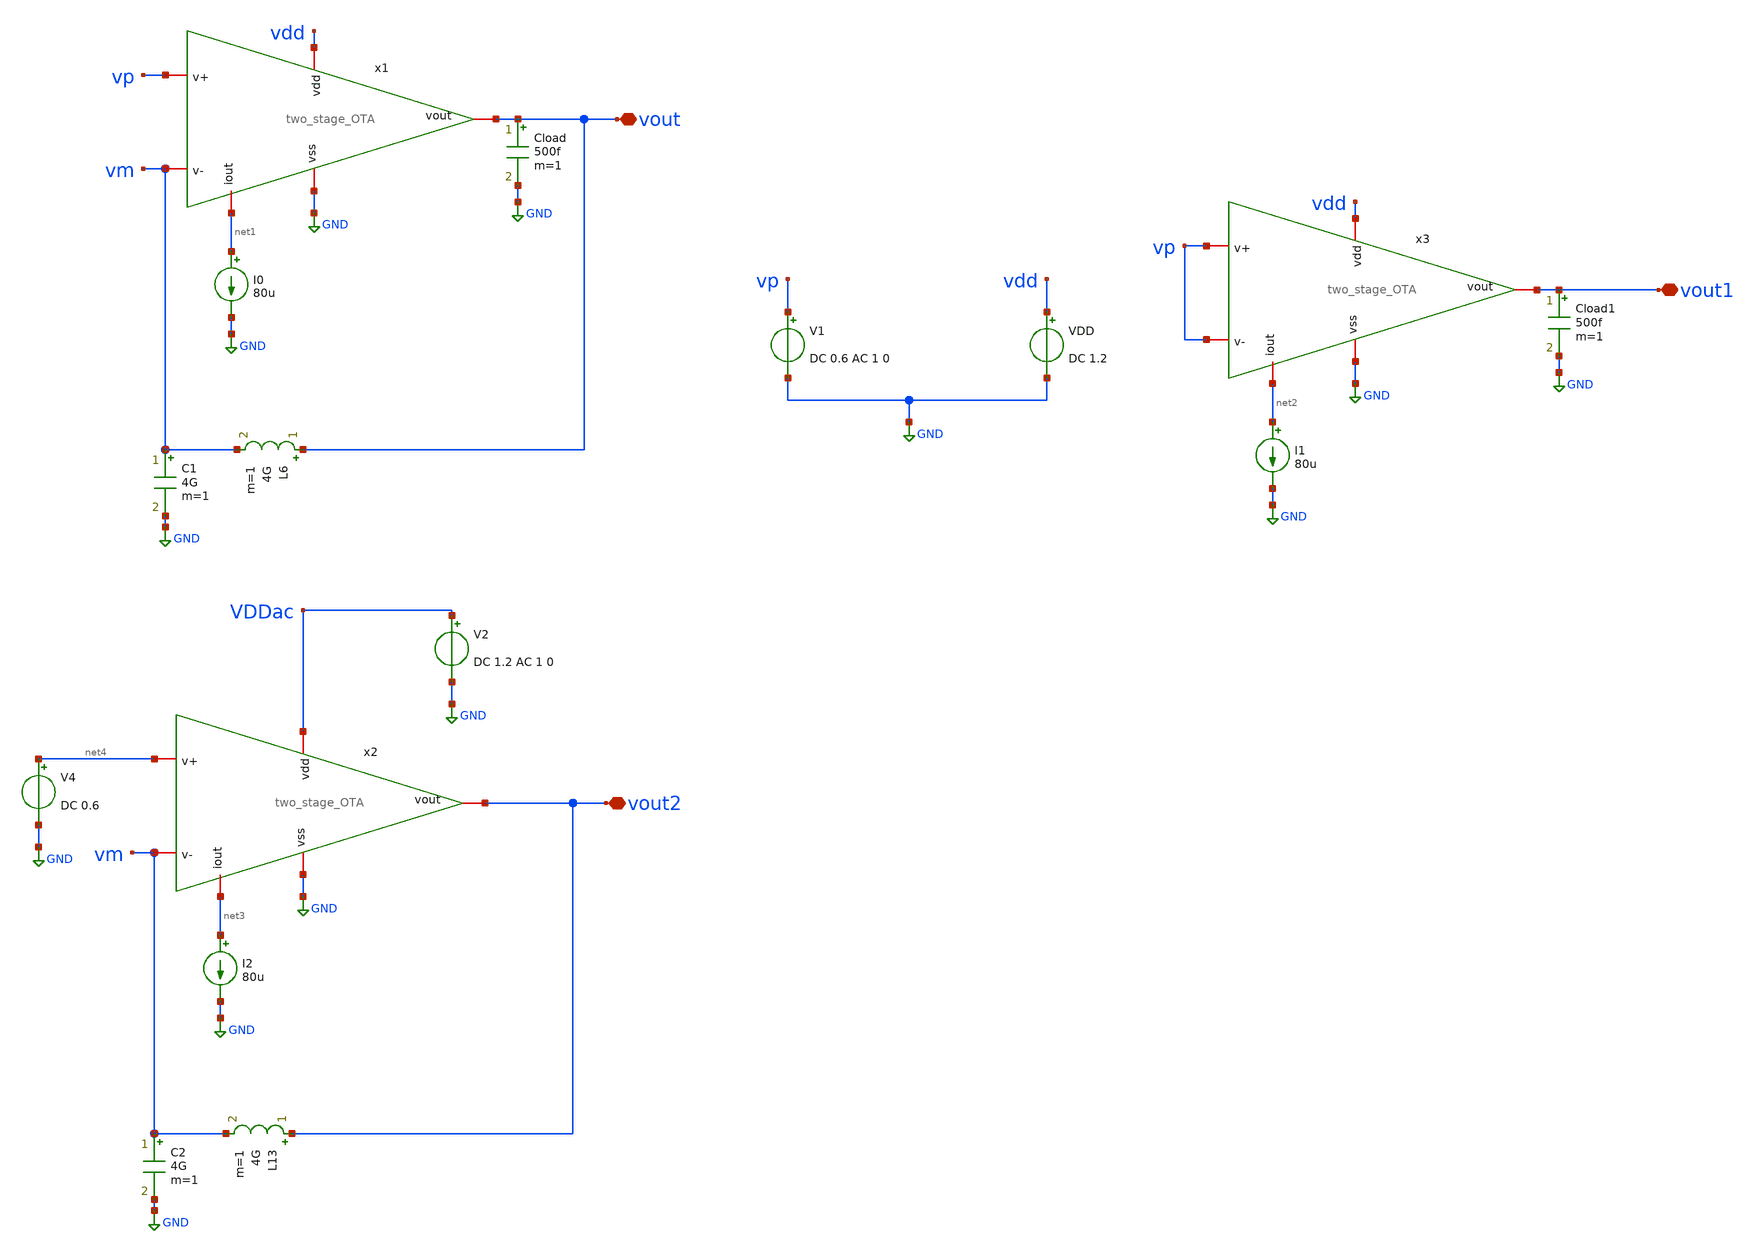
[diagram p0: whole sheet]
** sch_path: modules/module_1_bandgap_reference/part_1_OTA/testbenches/ota_testbench.sch
**.subckt ota_testbench vout vout1 vout2
*.iopin vout
*.iopin vout1
*.iopin vout2
V1 vp GND DC 0.6 AC 1 0
VDD vdd GND DC 1.2
I0 net1 GND 80u
Cload vout GND 500f m=1
L6 vout vm 4G m=1
C1 vm GND 4G m=1
I1 net2 GND 80u
Cload1 vout1 GND 500f m=1
I2 net3 GND 80u
L13 vout2 vm 4G m=1
C2 vm GND 4G m=1
V2 VDDac GND DC 1.2 AC 1 0
V4 net4 GND DC 0.6
x1 vdd net1 vp vm vout GND two_stage_OTA
x2 VDDac net3 net4 vm vout2 GND two_stage_OTA
x3 vdd net2 vp vp vout1 GND two_stage_OTA
**** begin user architecture code

.lib $::SG13G2_MODELS/cornerCAP.lib cap_typ
.lib cornerMOSlv.lib mos_tt



.control
op
save all
write tb_OTA_op.raw
.endc

.control
op
ac dec 100 1 10e6
save all
let Av = db(v(vout))
let PSRR_linear = v(vout2)/v(VDDac)
let CMRR = db((v(vout)/v(vp))/(v(vout1)/v(vp)))
let phase = 180*cph(vout)/pi
write output_file.raw
.endc


**** end user architecture code
**.ends

* expanding   symbol:  two_stage_OTA.sym # of pins=6
** sym_path: modules/module_1_bandgap_reference/part_1_OTA/gmid_example/schematic/two_stage_OTA.sym
** sch_path: modules/module_1_bandgap_reference/part_1_OTA/gmid_example/schematic/two_stage_OTA.sch
.subckt two_stage_OTA vdd iout v+ v- vout vss
*.iopin v-
*.iopin v+
*.iopin vss
*.iopin vdd
*.iopin iout
*.iopin vout
XM4 vout net1 vss vss sg13_lv_nmos w=3.09u l=6.24u ng=1 m=1 mm_ok=1
XM3 net1 net1 vss vss sg13_lv_nmos w=3.09u l=6.24u ng=1 m=1 mm_ok=1
XM1 net1 v+ net2 vdd sg13_lv_pmos w=2.75u l=5.46u ng=1 m=1 mm_ok=1
XM5 net2 iout vdd vdd sg13_lv_pmos w=66u l=9.98u ng=10 m=1 mm_ok=1
XM6 iout iout vdd vdd sg13_lv_pmos w=66u l=9.98u ng=10 m=1 mm_ok=1
XM2 vout v- net2 vdd sg13_lv_pmos w=2.75u l=5.46u ng=1 m=1 mm_ok=1
.ends

.GLOBAL GND
.end
